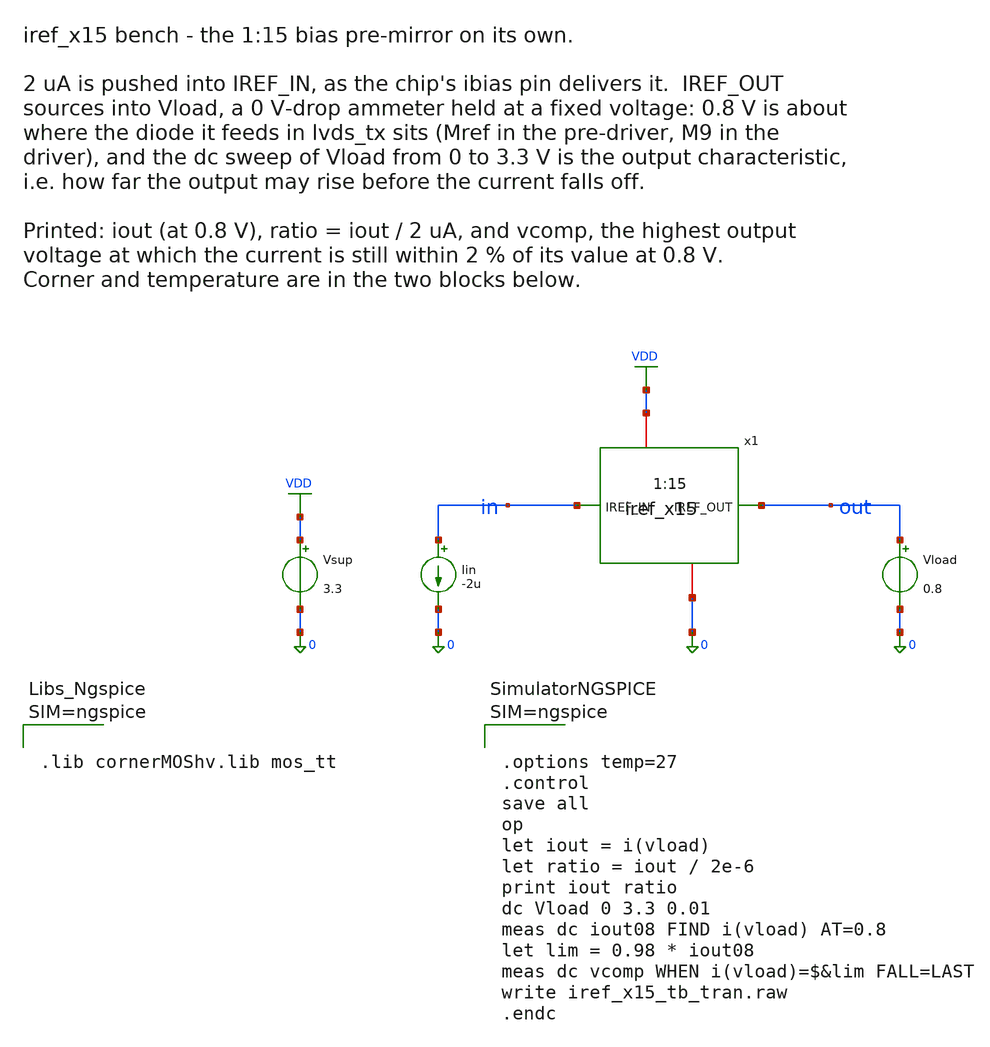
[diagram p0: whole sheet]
** sch_path: macros/iref_x15/testbenches/xschem/iref_x15_tb_tran.sch
**.subckt iref_x15_tb_tran
x1 in out VDD 0 iref_x15
Iin in 0 -2u
Vload out 0 0.8
.save i(vload)
Vsup VDD 0 3.3
**** begin user architecture code



.lib cornerMOShv.lib mos_tt






.options temp=27
.control
save all
op
let iout = i(vload)
let ratio = iout / 2e-6
print iout ratio
dc Vload 0 3.3 0.01
meas dc iout08 FIND i(vload) AT=0.8
let lim = 0.98 * iout08
meas dc vcomp WHEN i(vload)=$&lim FALL=LAST
write iref_x15_tb_tran.raw
.endc



**** end user architecture code
**.ends

* expanding   symbol:  iref_x15.sym # of pins=4
** sym_path: macros/iref_x15/schematic/xschem/iref_x15.sym
** sch_path: macros/iref_x15/schematic/xschem/iref_x15.sch
.subckt iref_x15 IREF_IN IREF_OUT Va Vss
*.ipin IREF_IN
*.opin IREF_OUT
*.iopin Va
*.iopin Vss
XMn1 IREF_IN IREF_IN Vss Vss sg13_hv_nmos w=3.2u l=2u ng=1 m=1 mm_ok=1
XMn2 CASC IREF_IN Vss Vss sg13_hv_nmos w=48u l=2u ng=6 m=1 mm_ok=1
XMp1 CASC CASC Va Va sg13_hv_pmos w=48u l=2u ng=6 m=1 mm_ok=1
XMp2 IREF_OUT CASC Va Va sg13_hv_pmos w=48u l=2u ng=6 m=1 mm_ok=1
.ends

.GLOBAL VDD
.end
